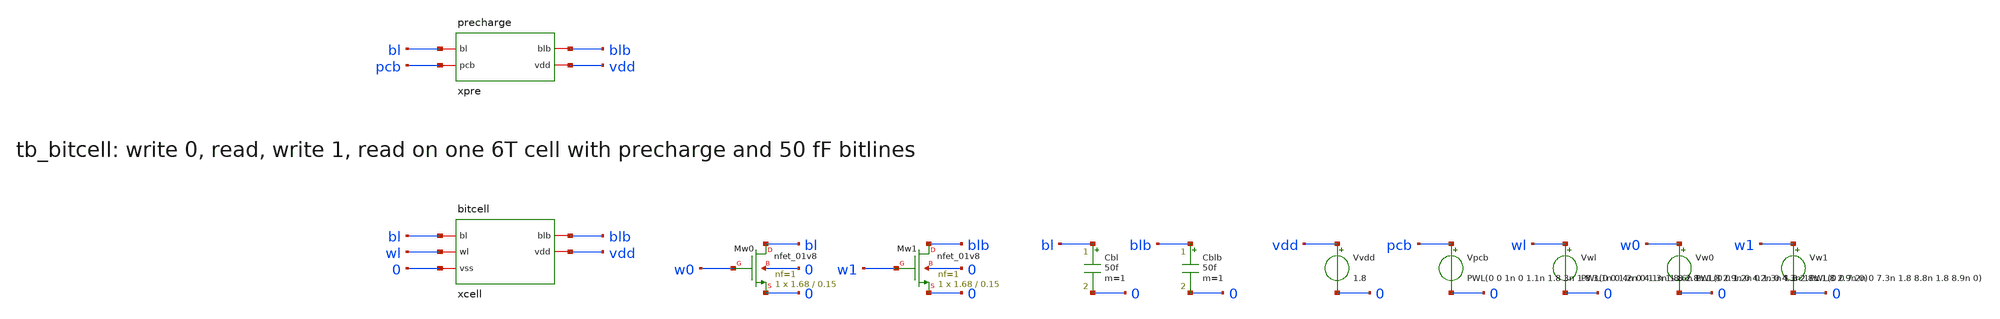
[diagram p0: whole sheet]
** sch_path: sram/xschem/tb_bitcell.sch
**.subckt tb_bitcell
xcell bl blb wl vdd 0 bitcell
xpre bl blb pcb vdd precharge
XMw0 bl w0 0 0 sky130_fd_pr__nfet_01v8 L=0.15 W=1.68 nf=1 ad='int((1 + 1)/2) * 1.68 / 1 * 0.29' as='int((1 + 2)/2) * 1.68 / 1 * 0.29'
+ pd='2*int((1 + 1)/2) * (1.68 / 1 + 0.29)' ps='2*int((1 + 2)/2) * (1.68 / 1 + 0.29)' nrd='0.29 / 1.68 '
+ nrs='0.29 / 1.68 ' sa=0 sb=0 sd=0 mult=1 m=1
XMw1 blb w1 0 0 sky130_fd_pr__nfet_01v8 L=0.15 W=1.68 nf=1 ad='int((1 + 1)/2) * 1.68 / 1 * 0.29' as='int((1 + 2)/2) * 1.68 / 1 * 0.29'
+ pd='2*int((1 + 1)/2) * (1.68 / 1 + 0.29)' ps='2*int((1 + 2)/2) * (1.68 / 1 + 0.29)' nrd='0.29 / 1.68 '
+ nrs='0.29 / 1.68 ' sa=0 sb=0 sd=0 mult=1 m=1
Cbl bl 0 50f m=1
Cblb blb 0 50f m=1
Vvdd vdd 0 1.8
Vpcb pcb 0 PWL(0 0 1n 0 1.1n 1.8 3n 1.8 3.1n 0 4n 0 4.1n 1.8 6n 1.8 6.1n 0 7n 0 7.1n 1.8 9n 1.8 9.1n
+ 0 10n 0 10.1n 1.8 12n 1.8 12.1n 0)
Vwl wl 0 PWL(0 0 1.2n 0 1.3n 1.8 2.8n 1.8 2.9n 0 4.2n 0 4.3n 1.8 5.8n 1.8 5.9n 0 7.2n 0 7.3n 1.8
+ 8.8n 1.8 8.9n 0 10.2n 0 10.3n 1.8 11.8n 1.8 11.9n 0)
Vw0 w0 0 PWL(0 0 1.2n 0 1.3n 1.8 2.8n 1.8 2.9n 0)
Vw1 w1 0 PWL(0 0 7.2n 0 7.3n 1.8 8.8n 1.8 8.9n 0)
**** begin user architecture code

.lib /foss/pdks/sky130A/libs.tech/ngspice/sky130.lib.spice tt
.ic v(xcell.q)=1.8 v(xcell.qb)=0
.tran 10p 12n
.control
run
set wr_singlescale
set wr_vecnames
wrdata tb_bitcell.dat v(xcell.q) v(xcell.qb) v(bl) v(blb) v(wl) v(pcb)
.endc

**** end user architecture code
**.ends

* expanding   symbol:  bitcell.sym # of pins=5
** sym_path: sram/xschem/bitcell.sym
** sch_path: sram/xschem/bitcell.sch
.subckt bitcell bl blb wl vdd vss
*.iopin bl
*.iopin blb
*.iopin wl
*.iopin vdd
*.iopin vss
XMPU1 q qb vdd vdd sky130_fd_pr__pfet_01v8 L=0.15 W=0.42 nf=1 ad='int((nf+1)/2) * W/nf * 0.29' as='int((nf+2)/2) * W/nf * 0.29'
+ pd='2*int((nf+1)/2) * (W/nf + 0.29)' ps='2*int((nf+2)/2) * (W/nf + 0.29)' nrd='0.29 / W' nrs='0.29 / W'
+ sa=0 sb=0 sd=0 mult=1 m=1
XMPD1 q qb vss vss sky130_fd_pr__nfet_01v8 L=0.15 W=0.63 nf=1 ad='int((1 + 1)/2) * 0.63 / 1 * 0.29' as='int((1 + 2)/2) * 0.63 / 1 * 0.29'
+ pd='2*int((1 + 1)/2) * (0.63 / 1 + 0.29)' ps='2*int((1 + 2)/2) * (0.63 / 1 + 0.29)' nrd='0.29 / 0.63 '
+ nrs='0.29 / 0.63 ' sa=0 sb=0 sd=0 mult=1 m=1
XMPU2 qb q vdd vdd sky130_fd_pr__pfet_01v8 L=0.15 W=0.42 nf=1 ad='int((nf+1)/2) * W/nf * 0.29' as='int((nf+2)/2) * W/nf * 0.29'
+ pd='2*int((nf+1)/2) * (W/nf + 0.29)' ps='2*int((nf+2)/2) * (W/nf + 0.29)' nrd='0.29 / W' nrs='0.29 / W'
+ sa=0 sb=0 sd=0 mult=1 m=1
XMPD2 qb q vss vss sky130_fd_pr__nfet_01v8 L=0.15 W=0.63 nf=1 ad='int((1 + 1)/2) * 0.63 / 1 * 0.29' as='int((1 + 2)/2) * 0.63 / 1 * 0.29'
+ pd='2*int((1 + 1)/2) * (0.63 / 1 + 0.29)' ps='2*int((1 + 2)/2) * (0.63 / 1 + 0.29)' nrd='0.29 / 0.63 '
+ nrs='0.29 / 0.63 ' sa=0 sb=0 sd=0 mult=1 m=1
XMPG1 bl wl q vss sky130_fd_pr__nfet_01v8 L=0.15 W=0.42 nf=1 ad='int((1 + 1)/2) * 0.42 / 1 * 0.29' as='int((1 + 2)/2) * 0.42 / 1 * 0.29'
+ pd='2*int((1 + 1)/2) * (0.42 / 1 + 0.29)' ps='2*int((1 + 2)/2) * (0.42 / 1 + 0.29)' nrd='0.29 / 0.42 '
+ nrs='0.29 / 0.42 ' sa=0 sb=0 sd=0 mult=1 m=1
XMPG2 blb wl qb vss sky130_fd_pr__nfet_01v8 L=0.15 W=0.42 nf=1 ad='int((1 + 1)/2) * 0.42 / 1 * 0.29'
+ as='int((1 + 2)/2) * 0.42 / 1 * 0.29' pd='2*int((1 + 1)/2) * (0.42 / 1 + 0.29)' ps='2*int((1 + 2)/2) * (0.42 / 1 + 0.29)'
+ nrd='0.29 / 0.42 ' nrs='0.29 / 0.42 ' sa=0 sb=0 sd=0 mult=1 m=1
.ends


* expanding   symbol:  precharge.sym # of pins=4
** sym_path: sram/xschem/precharge.sym
** sch_path: sram/xschem/precharge.sch
.subckt precharge bl blb pcb vdd
*.iopin bl
*.iopin blb
*.iopin pcb
*.iopin vdd
XMP1 bl pcb vdd vdd sky130_fd_pr__pfet_01v8 L=0.15 W=0.84 nf=1 ad='int((nf+1)/2) * W/nf * 0.29' as='int((nf+2)/2) * W/nf * 0.29'
+ pd='2*int((nf+1)/2) * (W/nf + 0.29)' ps='2*int((nf+2)/2) * (W/nf + 0.29)' nrd='0.29 / W' nrs='0.29 / W'
+ sa=0 sb=0 sd=0 mult=1 m=1
XMP2 blb pcb vdd vdd sky130_fd_pr__pfet_01v8 L=0.15 W=0.84 nf=1 ad='int((nf+1)/2) * W/nf * 0.29' as='int((nf+2)/2) * W/nf * 0.29'
+ pd='2*int((nf+1)/2) * (W/nf + 0.29)' ps='2*int((nf+2)/2) * (W/nf + 0.29)' nrd='0.29 / W' nrs='0.29 / W'
+ sa=0 sb=0 sd=0 mult=1 m=1
XMP3 bl pcb blb vdd sky130_fd_pr__pfet_01v8 L=0.15 W=0.42 nf=1 ad='int((nf+1)/2) * W/nf * 0.29' as='int((nf+2)/2) * W/nf * 0.29'
+ pd='2*int((nf+1)/2) * (W/nf + 0.29)' ps='2*int((nf+2)/2) * (W/nf + 0.29)' nrd='0.29 / W' nrs='0.29 / W'
+ sa=0 sb=0 sd=0 mult=1 m=1
.ends

.end
